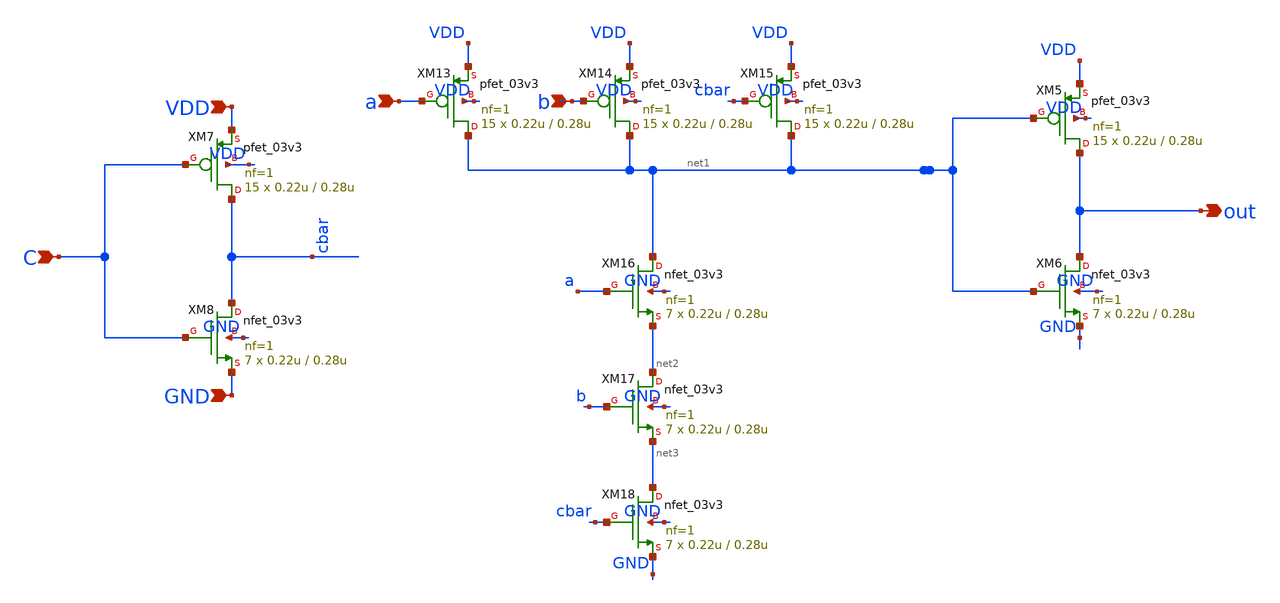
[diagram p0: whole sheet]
** sch_path: blocks/adc/encoder/sym/NAND3.sch
**.subckt NAND3 a out C b VDD GND
*.ipin a
*.opin out
*.ipin C
*.ipin b
*.ipin VDD
*.ipin GND
XM5 out net1 VDD VDD pfet_03v3 L=0.28u W=0.22u nf=1 ad='int((nf+1)/2) * W/nf * 0.18u' as='int((nf+2)/2) * W/nf * 0.18u'
+ pd='2*int((nf+1)/2) * (W/nf + 0.18u)' ps='2*int((nf+2)/2) * (W/nf + 0.18u)' nrd='0.18u / W' nrs='0.18u / W'
+ sa=0 sb=0 sd=0 m=15
XM6 out net1 GND GND nfet_03v3 L=0.28u W=0.22u nf=1 ad='int((nf+1)/2) * W/nf * 0.18u' as='int((nf+2)/2) * W/nf * 0.18u'
+ pd='2*int((nf+1)/2) * (W/nf + 0.18u)' ps='2*int((nf+2)/2) * (W/nf + 0.18u)' nrd='0.18u / W' nrs='0.18u / W'
+ sa=0 sb=0 sd=0 m=7
XM7 cbar C VDD VDD pfet_03v3 L=0.28u W=0.22u nf=1 ad='int((nf+1)/2) * W/nf * 0.18u' as='int((nf+2)/2) * W/nf * 0.18u'
+ pd='2*int((nf+1)/2) * (W/nf + 0.18u)' ps='2*int((nf+2)/2) * (W/nf + 0.18u)' nrd='0.18u / W' nrs='0.18u / W'
+ sa=0 sb=0 sd=0 m=15
XM8 cbar C GND GND nfet_03v3 L=0.28u W=0.22u nf=1 ad='int((nf+1)/2) * W/nf * 0.18u' as='int((nf+2)/2) * W/nf * 0.18u'
+ pd='2*int((nf+1)/2) * (W/nf + 0.18u)' ps='2*int((nf+2)/2) * (W/nf + 0.18u)' nrd='0.18u / W' nrs='0.18u / W'
+ sa=0 sb=0 sd=0 m=7
XM13 net1 a VDD VDD pfet_03v3 L=0.28u W=0.22u nf=1 ad='int((nf+1)/2) * W/nf * 0.18u' as='int((nf+2)/2) * W/nf * 0.18u'
+ pd='2*int((nf+1)/2) * (W/nf + 0.18u)' ps='2*int((nf+2)/2) * (W/nf + 0.18u)' nrd='0.18u / W' nrs='0.18u / W'
+ sa=0 sb=0 sd=0 m=15
XM14 net1 b VDD VDD pfet_03v3 L=0.28u W=0.22u nf=1 ad='int((nf+1)/2) * W/nf * 0.18u' as='int((nf+2)/2) * W/nf * 0.18u'
+ pd='2*int((nf+1)/2) * (W/nf + 0.18u)' ps='2*int((nf+2)/2) * (W/nf + 0.18u)' nrd='0.18u / W' nrs='0.18u / W'
+ sa=0 sb=0 sd=0 m=15
XM15 net1 cbar VDD VDD pfet_03v3 L=0.28u W=0.22u nf=1 ad='int((nf+1)/2) * W/nf * 0.18u' as='int((nf+2)/2) * W/nf * 0.18u'
+ pd='2*int((nf+1)/2) * (W/nf + 0.18u)' ps='2*int((nf+2)/2) * (W/nf + 0.18u)' nrd='0.18u / W' nrs='0.18u / W'
+ sa=0 sb=0 sd=0 m=15
XM16 net1 a net2 GND nfet_03v3 L=0.28u W=0.22u nf=1 ad='int((nf+1)/2) * W/nf * 0.18u' as='int((nf+2)/2) * W/nf * 0.18u'
+ pd='2*int((nf+1)/2) * (W/nf + 0.18u)' ps='2*int((nf+2)/2) * (W/nf + 0.18u)' nrd='0.18u / W' nrs='0.18u / W'
+ sa=0 sb=0 sd=0 m=7
XM17 net2 b net3 GND nfet_03v3 L=0.28u W=0.22u nf=1 ad='int((nf+1)/2) * W/nf * 0.18u' as='int((nf+2)/2) * W/nf * 0.18u'
+ pd='2*int((nf+1)/2) * (W/nf + 0.18u)' ps='2*int((nf+2)/2) * (W/nf + 0.18u)' nrd='0.18u / W' nrs='0.18u / W'
+ sa=0 sb=0 sd=0 m=7
XM18 net3 cbar GND GND nfet_03v3 L=0.28u W=0.22u nf=1 ad='int((nf+1)/2) * W/nf * 0.18u' as='int((nf+2)/2) * W/nf * 0.18u'
+ pd='2*int((nf+1)/2) * (W/nf + 0.18u)' ps='2*int((nf+2)/2) * (W/nf + 0.18u)' nrd='0.18u / W' nrs='0.18u / W'
+ sa=0 sb=0 sd=0 m=7
**.ends
.end
